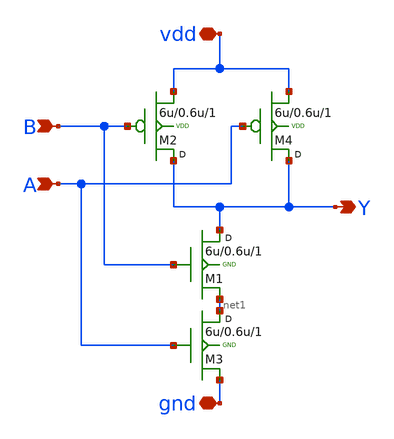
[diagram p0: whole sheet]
** sch_path: Tutorials/1-4_StdCell_DFFSR/Sch/NAND2X1.sch
**.subckt NAND2X1 A B Y vdd gnd
*.ipin A
*.ipin B
*.opin Y
*.iopin vdd
*.iopin gnd
M1 Y B net1 GND nfet w=6u l=0.6u m=1
M2 Y B vdd VDD pfet w=6u l=0.6u m=1
M3 net1 A gnd GND nfet w=6u l=0.6u m=1
M4 Y A vdd VDD pfet w=6u l=0.6u m=1
**.ends
.end
